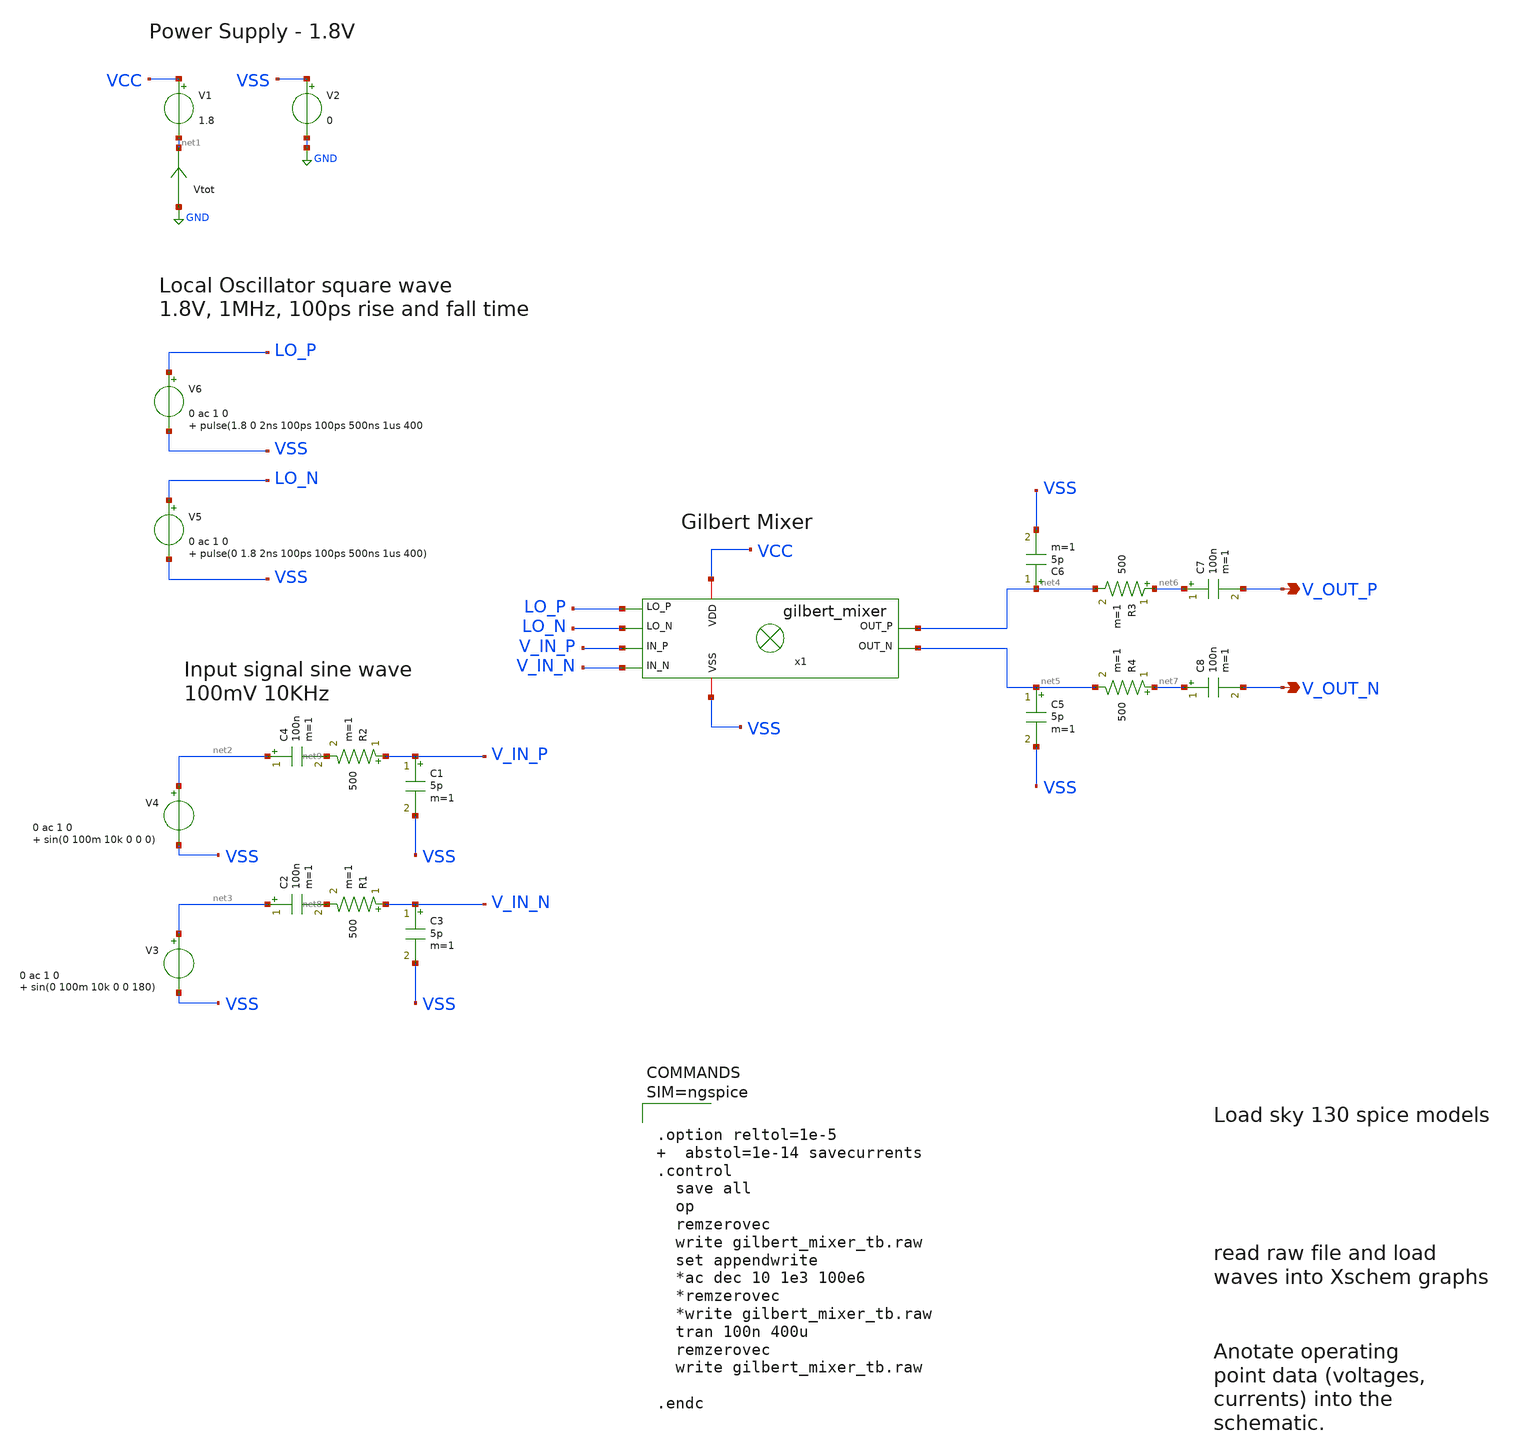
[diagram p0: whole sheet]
** sch_path: xschem/gilbert_mixer_tb.sch
**.subckt gilbert_mixer_tb V_OUT_N V_OUT_P
*.opin V_OUT_N
*.opin V_OUT_P
V1 VCC net1 1.8
V2 VSS GND 0
V4 net2 VSS 0 ac 1 0 sin(0 100m 10k 0 0 0)
x1 VSS VCC net5 net4 LO_N LO_P V_IN_N V_IN_P gilbert_mixer
V5 LO_N VSS 0 ac 1 0 pulse(0 1.8 2ns 100ps 100ps 500ns 1us 400)
V3 net3 VSS 0 ac 1 0 sin(0 100m 10k 0 0 180)
Vtot GND net1 0
.save i(vtot)
V6 LO_P VSS 0 ac 1 0 pulse(1.8 0 2ns 100ps 100ps 500ns 1us 400
R1 V_IN_N net8 500 m=1
R2 V_IN_P net9 500 m=1
R3 net6 net4 500 m=1
R4 net7 net5 500 m=1
C1 V_IN_P VSS 5p m=1
C3 V_IN_N VSS 5p m=1
C5 net5 VSS 5p m=1
C6 net4 VSS 5p m=1
C4 net2 net9 100n m=1
C2 net3 net8 100n m=1
C7 net6 V_OUT_P 100n m=1
C8 net7 V_OUT_N 100n m=1
**** begin user architecture code

** opencircuitdesign pdks install
.lib $::SKYWATER_MODELS/sky130.lib.spice tt





.option reltol=1e-5   abstol=1e-14 savecurrents
.control
  save all
  op
  remzerovec
  write gilbert_mixer_tb.raw
  set appendwrite
  *ac dec 10 1e3 100e6
  *remzerovec
  *write gilbert_mixer_tb.raw
  tran 100n 400u
  remzerovec
  write gilbert_mixer_tb.raw

.endc



**** end user architecture code
**.ends

* expanding   symbol:  gilbert_mixer.sym # of pins=8
** sym_path: xschem/gilbert_mixer.sym
** sch_path: xschem/gilbert_mixer.sch
.subckt gilbert_mixer VSS VDD OUT_N OUT_P LO_N LO_P IN_N IN_P
*.ipin LO_P
*.ipin LO_N
*.ipin IN_N
*.opin OUT_N
*.opin OUT_P
*.iopin VDD
*.iopin VSS
*.ipin IN_P
XR3 VSS NET_R3 VSS sky130_fd_pr__res_high_po_0p35 L=0.1 mult=30 m=30
XM2 OUT_P IN_N NET_M6_DRAIN VSS sky130_fd_pr__nfet_01v8 L=0.38 W=3.6 nf=2 ad='int((nf+1)/2) * W/nf * 0.29'
+ as='int((nf+2)/2) * W/nf * 0.29' pd='2*int((nf+1)/2) * (W/nf + 0.29)' ps='2*int((nf+2)/2) * (W/nf + 0.29)'
+ nrd='0.29 / W' nrs='0.29 / W' sa=0 sb=0 sd=0 mult=1 m=1
XM4 OUT_N IN_N NET_M5_DRAIN VSS sky130_fd_pr__nfet_01v8 L=0.38 W=3.6 nf=2 ad='int((nf+1)/2) * W/nf * 0.29'
+ as='int((nf+2)/2) * W/nf * 0.29' pd='2*int((nf+1)/2) * (W/nf + 0.29)' ps='2*int((nf+2)/2) * (W/nf + 0.29)'
+ nrd='0.29 / W' nrs='0.29 / W' sa=0 sb=0 sd=0 mult=1 m=1
XM6 NET_M6_DRAIN LO_N NET_R3 VSS sky130_fd_pr__nfet_01v8 L=0.38 W=3.6 nf=2 ad='int((nf+1)/2) * W/nf * 0.29'
+ as='int((nf+2)/2) * W/nf * 0.29' pd='2*int((nf+1)/2) * (W/nf + 0.29)' ps='2*int((nf+2)/2) * (W/nf + 0.29)'
+ nrd='0.29 / W' nrs='0.29 / W' sa=0 sb=0 sd=0 mult=1 m=1
XM1 OUT_N IN_P NET_M6_DRAIN VSS sky130_fd_pr__nfet_01v8 L=0.38 W=3.6 nf=2 ad='int((nf+1)/2) * W/nf * 0.29'
+ as='int((nf+2)/2) * W/nf * 0.29' pd='2*int((nf+1)/2) * (W/nf + 0.29)' ps='2*int((nf+2)/2) * (W/nf + 0.29)'
+ nrd='0.29 / W' nrs='0.29 / W' sa=0 sb=0 sd=0 mult=1 m=1
XM3 OUT_P IN_P NET_M5_DRAIN VSS sky130_fd_pr__nfet_01v8 L=0.38 W=3.6 nf=2 ad='int((nf+1)/2) * W/nf * 0.29'
+ as='int((nf+2)/2) * W/nf * 0.29' pd='2*int((nf+1)/2) * (W/nf + 0.29)' ps='2*int((nf+2)/2) * (W/nf + 0.29)'
+ nrd='0.29 / W' nrs='0.29 / W' sa=0 sb=0 sd=0 mult=1 m=1
XM5 NET_M5_DRAIN LO_P NET_R3 VSS sky130_fd_pr__nfet_01v8 L=0.38 W=3.6 nf=2 ad='int((nf+1)/2) * W/nf * 0.29'
+ as='int((nf+2)/2) * W/nf * 0.29' pd='2*int((nf+1)/2) * (W/nf + 0.29)' ps='2*int((nf+2)/2) * (W/nf + 0.29)'
+ nrd='0.29 / W' nrs='0.29 / W' sa=0 sb=0 sd=0 mult=1 m=1
XR1 OUT_N VDD VSS sky130_fd_pr__res_high_po_0p35 L=15.3 mult=2 m=2
XR2 OUT_P VDD VSS sky130_fd_pr__res_high_po_0p35 L=15.3 mult=2 m=2
XR4 IN_N VDD VSS sky130_fd_pr__res_high_po_0p35 L=6 mult=2 m=2
XR5 VSS IN_N VSS sky130_fd_pr__res_high_po_0p35 L=7 mult=2 m=2
XR6 IN_P VDD VSS sky130_fd_pr__res_high_po_0p35 L=6 mult=2 m=2
XR7 VSS IN_P VSS sky130_fd_pr__res_high_po_0p35 L=7 mult=2 m=2
.ends

.GLOBAL GND
.end
